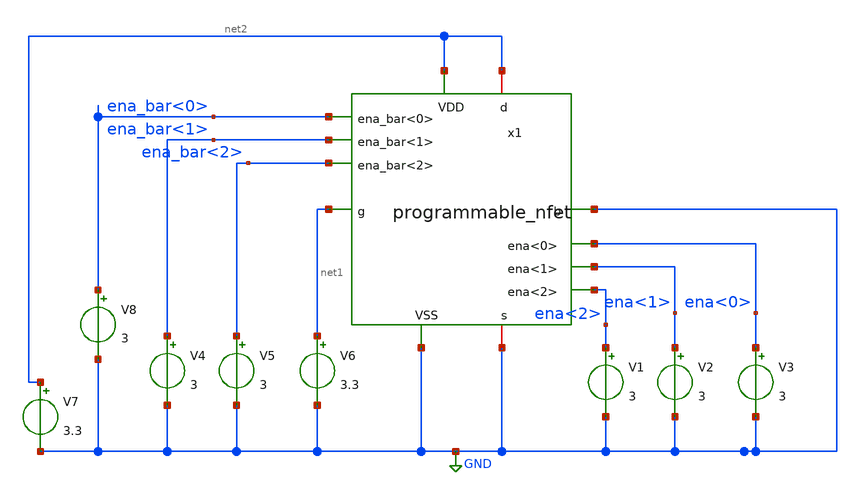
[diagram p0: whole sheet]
** sch_path: designs/libs/core_digital/TB_prog_fet.sch
**.subckt TB_prog_fet
V1 ena<2> GND 3
V2 ena<1> GND 3
V3 ena<0> GND 3
V4 ena_bar<1> GND 3
V5 ena_bar<2> GND 3
V6 net1 GND 3.3
V7 net2 GND 3.3
V8 ena_bar<0> GND 3
x1 ena_bar<1> net2 net1 GND ena_bar<0> GND net2 ena_bar<2> ena<0> GND ena<1> ena<2>
+ programmable_nfet width=0.22u length=0.28u
**.ends

* expanding   symbol:  libs/core_digital/programmable_nfet.sym # of pins=12
** sym_path: designs/libs/core_digital/programmable_nfet.sym
** sch_path: designs/libs/core_digital/programmable_nfet.sch
.subckt programmable_nfet ena_bar<1> d g b ena_bar<0> s VDD ena_bar<2> ena<0> VSS ena<1> ena<2>
+  width=0.22u length=0.28u
*.ipin VSS
*.ipin VDD
*.ipin g
*.ipin ena_bar<1>
*.ipin ena_bar<0>
*.ipin ena_bar<2>
*.ipin ena<2>
*.ipin ena<0>
*.ipin ena<1>
*.iopin d
*.iopin s
*.ipin b
XM1 d net3 s b nfet_03v3 L={length} W={width} nf=1 ad='int((nf+1)/2) * W/nf * 0.18u' as='int((nf+2)/2) * W/nf * 0.18u'
+ pd='2*int((nf+1)/2) * (W/nf + 0.18u)' ps='2*int((nf+2)/2) * (W/nf + 0.18u)' nrd='0.18u / W' nrs='0.18u / W'
+ sa=0 sb=0 sd=0 m=1
XM2 d net2 s b nfet_03v3 L={length} W={width} nf=1 ad='int((nf+1)/2) * W/nf * 0.18u' as='int((nf+2)/2) * W/nf * 0.18u'
+ pd='2*int((nf+1)/2) * (W/nf + 0.18u)' ps='2*int((nf+2)/2) * (W/nf + 0.18u)' nrd='0.18u / W' nrs='0.18u / W'
+ sa=0 sb=0 sd=0 m=1
XM3 d net1 s b nfet_03v3 L={length} W=2*{width} nf=1 ad='int((nf+1)/2) * W/nf * 0.18u' as='int((nf+2)/2) * W/nf * 0.18u'
+ pd='2*int((nf+1)/2) * (W/nf + 0.18u)' ps='2*int((nf+2)/2) * (W/nf + 0.18u)' nrd='0.18u / W' nrs='0.18u / W'
+ sa=0 sb=0 sd=0 m=1
x1 ena_bar<0> VDD net3 g VSS ena<0> transmission_gate
x2 ena_bar<1> VDD net2 g VSS ena<1> transmission_gate
x3 ena_bar<2> VDD net1 g VSS ena<2> transmission_gate
.ends


* expanding   symbol:  libs/core_digital/transmission_gate.sym # of pins=6
** sym_path: designs/libs/core_digital/schem/transmission_gate.sym
** sch_path: designs/libs/core_digital/schem/transmission_gate.sch
.subckt transmission_gate ena_bar VDD out in VSS ena
*.ipin in
*.ipin ena_bar
*.ipin ena
*.ipin VSS
*.ipin VDD
*.opin out
XM1 in ena_bar out VDD pfet_03v3 L=0.28u W=0.22u nf=1 ad='int((nf+1)/2) * W/nf * 0.18u' as='int((nf+2)/2) * W/nf * 0.18u'
+ pd='2*int((nf+1)/2) * (W/nf + 0.18u)' ps='2*int((nf+2)/2) * (W/nf + 0.18u)' nrd='0.18u / W' nrs='0.18u / W'
+ sa=0 sb=0 sd=0 m=1
XM2 in ena out VSS nfet_03v3 L=0.28u W=0.22u nf=1 ad='int((nf+1)/2) * W/nf * 0.18u' as='int((nf+2)/2) * W/nf * 0.18u'
+ pd='2*int((nf+1)/2) * (W/nf + 0.18u)' ps='2*int((nf+2)/2) * (W/nf + 0.18u)' nrd='0.18u / W' nrs='0.18u / W'
+ sa=0 sb=0 sd=0 m=1
.ends

.GLOBAL GND
.end
